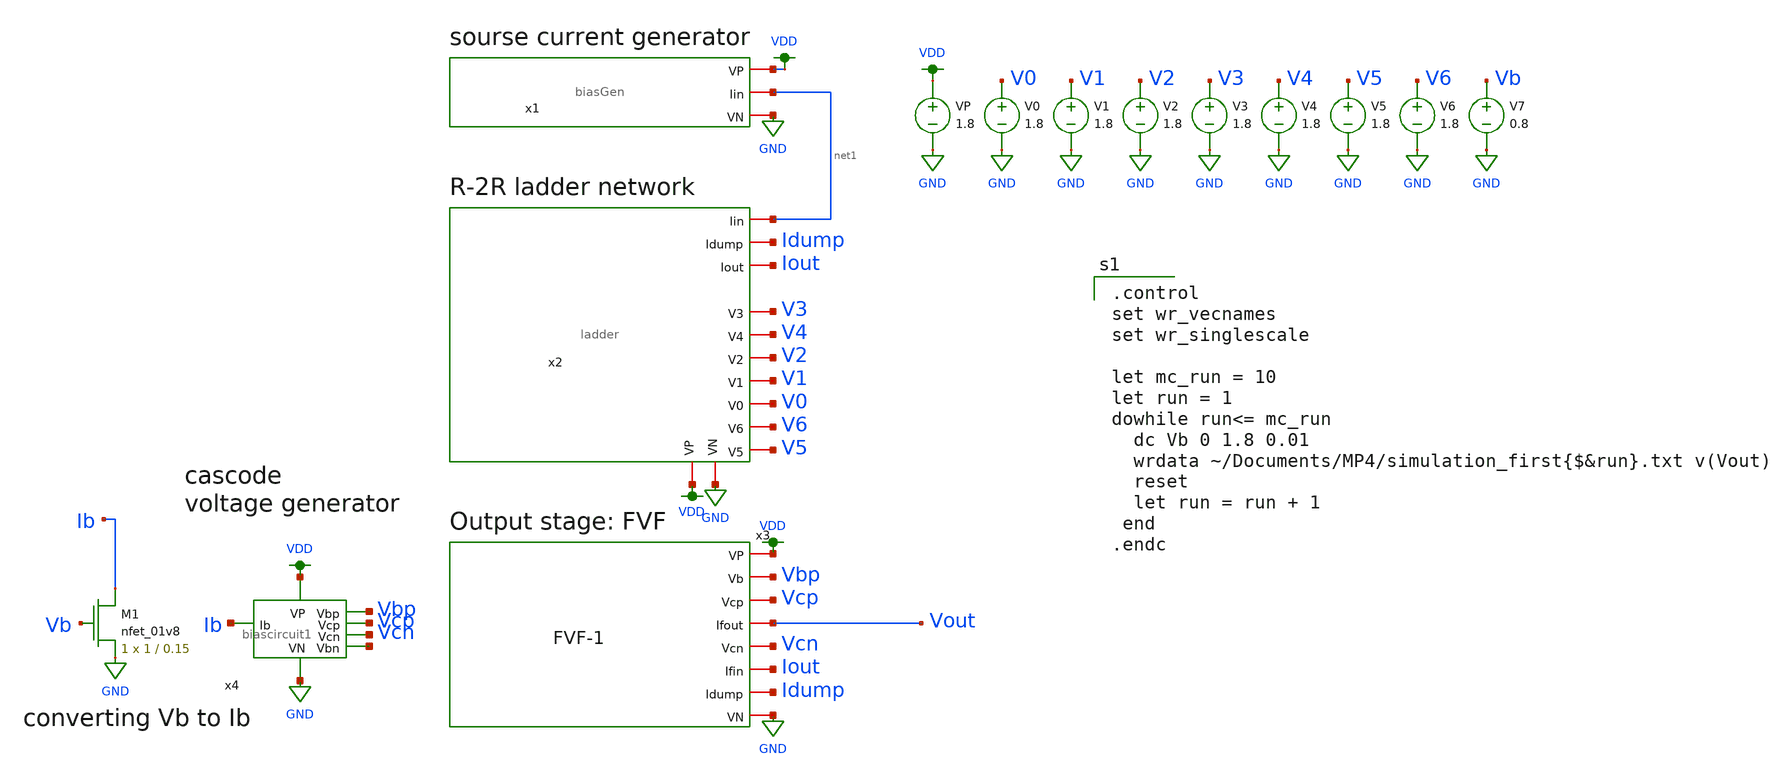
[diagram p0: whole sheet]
** sch_path: MP4-simulation-1.sch
**.subckt MP4-simulation-1
x1 VDD net1 GND biasGen
V1 V1 GND 1.8
V2 V2 GND 1.8
V3 V3 GND 1.8
V4 V4 GND 1.8
V5 V5 GND 1.8
V6 V6 GND 1.8
V0 V0 GND 1.8
VP VDD GND 1.8
V7 Vb GND 0.8
x2 net1 Idump Iout V3 V4 V2 V1 V0 V6 V5 GND VDD ladder
x4 Vbp Vcn Vcp net2 Ib GND VDD biascircuit1
x3 VDD Vbp Vcp Vout Vcn Iout Idump GND FVF-1
XM1 Ib Vb GND GND sky130_fd_pr__nfet_01v8 L=0.15 W=1 nf=1 ad='int((nf+1)/2) * W/nf * 0.29' as='int((nf+2)/2) * W/nf * 0.29'
+ pd='2*int((nf+1)/2) * (W/nf + 0.29)' ps='2*int((nf+2)/2) * (W/nf + 0.29)' nrd='0.29 / W' nrs='0.29 / W'
+ sa=0 sb=0 sd=0 mult=1 m=1
**** begin user architecture code

.option wnflag=1
.param MC_SWITCH=0.0
.lib ~/skywater/skywater-pdk/libraries/sky130_fd_pr_ngspice/latest/models/sky130.lib.spice tt


.control
set wr_vecnames
set wr_singlescale

let mc_run = 10
let run = 1
dowhile run<= mc_run
  dc Vb 0 1.8 0.01
  wrdata ~/Documents/MP4/simulation_first{$&run}.txt v(Vout)
  reset
  let run = run + 1
 end
.endc

**** end user architecture code
**.ends

* expanding   symbol:  ./biasGen.sym # of pins=3
** sym_path: biasGen.sym
** sch_path: biasGen.sch
.subckt biasGen VP Iin VN
*.iopin VN
*.iopin Iin
*.iopin VP
XM1 net4 net4 VN GND sky130_fd_pr__nfet_01v8 L=0.15 W=1 nf=1 ad='int((nf+1)/2) * W/nf * 0.29' as='int((nf+2)/2) * W/nf * 0.29'
+ pd='2*int((nf+1)/2) * (W/nf + 0.29)' ps='2*int((nf+2)/2) * (W/nf + 0.29)' nrd='0.29 / W' nrs='0.29 / W'
+ sa=0 sb=0 sd=0 mult=1 m=1
XM2 VN net4 net3 GND sky130_fd_pr__nfet_01v8 L=0.15 W=1 nf=1 ad='int((nf+1)/2) * W/nf * 0.29' as='int((nf+2)/2) * W/nf * 0.29'
+ pd='2*int((nf+1)/2) * (W/nf + 0.29)' ps='2*int((nf+2)/2) * (W/nf + 0.29)' nrd='0.29 / W' nrs='0.29 / W'
+ sa=0 sb=0 sd=0 mult=1 m=1
XM3 net1 net2 VN GND sky130_fd_pr__nfet_01v8 L=0.15 W=1 nf=1 ad='int((nf+1)/2) * W/nf * 0.29' as='int((nf+2)/2) * W/nf * 0.29'
+ pd='2*int((nf+1)/2) * (W/nf + 0.29)' ps='2*int((nf+2)/2) * (W/nf + 0.29)' nrd='0.29 / W' nrs='0.29 / W'
+ sa=0 sb=0 sd=0 mult=1 m=1
XM4 net5 net2 net2 GND sky130_fd_pr__nfet_01v8 L=0.15 W=8 nf=1 ad='int((nf+1)/2) * W/nf * 0.29' as='int((nf+2)/2) * W/nf * 0.29'
+ pd='2*int((nf+1)/2) * (W/nf + 0.29)' ps='2*int((nf+2)/2) * (W/nf + 0.29)' nrd='0.29 / W' nrs='0.29 / W'
+ sa=0 sb=0 sd=0 mult=1 m=1
XM5 net3 net1 VP VDD sky130_fd_pr__pfet_01v8 L=0.15 W=1 nf=1 ad='int((nf+1)/2) * W/nf * 0.29' as='int((nf+2)/2) * W/nf * 0.29'
+ pd='2*int((nf+1)/2) * (W/nf + 0.29)' ps='2*int((nf+2)/2) * (W/nf + 0.29)' nrd='0.29 / W' nrs='0.29 / W'
+ sa=0 sb=0 sd=0 mult=1 m=1
XM6 VP net1 net1 VDD sky130_fd_pr__pfet_01v8 L=0.15 W=1 nf=1 ad='int((nf+1)/2) * W/nf * 0.29' as='int((nf+2)/2) * W/nf * 0.29'
+ pd='2*int((nf+1)/2) * (W/nf + 0.29)' ps='2*int((nf+2)/2) * (W/nf + 0.29)' nrd='0.29 / W' nrs='0.29 / W'
+ sa=0 sb=0 sd=0 mult=1 m=1
XM7 VP net3 net2 VDD sky130_fd_pr__pfet_01v8 L=0.15 W=1 nf=1 ad='int((nf+1)/2) * W/nf * 0.29' as='int((nf+2)/2) * W/nf * 0.29'
+ pd='2*int((nf+1)/2) * (W/nf + 0.29)' ps='2*int((nf+2)/2) * (W/nf + 0.29)' nrd='0.29 / W' nrs='0.29 / W'
+ sa=0 sb=0 sd=0 mult=1 m=1
XM8 net4 net3 VP VDD sky130_fd_pr__pfet_01v8 L=0.15 W=1 nf=1 ad='int((nf+1)/2) * W/nf * 0.29' as='int((nf+2)/2) * W/nf * 0.29'
+ pd='2*int((nf+1)/2) * (W/nf + 0.29)' ps='2*int((nf+2)/2) * (W/nf + 0.29)' nrd='0.29 / W' nrs='0.29 / W'
+ sa=0 sb=0 sd=0 mult=1 m=1
R1 net5 VN 100k m=1
XM9 Iin net3 VP VDD sky130_fd_pr__pfet_01v8 L=0.15 W=1 nf=1 ad='int((nf+1)/2) * W/nf * 0.29' as='int((nf+2)/2) * W/nf * 0.29'
+ pd='2*int((nf+1)/2) * (W/nf + 0.29)' ps='2*int((nf+2)/2) * (W/nf + 0.29)' nrd='0.29 / W' nrs='0.29 / W'
+ sa=0 sb=0 sd=0 mult=1 m=1
.ends


* expanding   symbol:  ./ladder.sym # of pins=12
** sym_path: ladder.sym
** sch_path: ladder.sch
.subckt ladder Iin Idump Iout V3 V4 V2 V1 V0 V6 V5 VN VP
*.iopin VP
*.iopin Iin
*.iopin V0
*.iopin V1
*.iopin V2
*.iopin V3
*.iopin V4
*.iopin V5
*.iopin V6
*.iopin VN
*.iopin Idump
*.iopin Iout
XM1 Iin VP net1 GND sky130_fd_pr__nfet_01v8 L=0.15 W=1 nf=1 ad='int((nf+1)/2) * W/nf * 0.29' as='int((nf+2)/2) * W/nf * 0.29'
+ pd='2*int((nf+1)/2) * (W/nf + 0.29)' ps='2*int((nf+2)/2) * (W/nf + 0.29)' nrd='0.29 / W' nrs='0.29 / W'
+ sa=0 sb=0 sd=0 mult=1 m=1
XM3 Iin VP net3 GND sky130_fd_pr__nfet_01v8 L=0.15 W=1 nf=1 ad='int((nf+1)/2) * W/nf * 0.29' as='int((nf+2)/2) * W/nf * 0.29'
+ pd='2*int((nf+1)/2) * (W/nf + 0.29)' ps='2*int((nf+2)/2) * (W/nf + 0.29)' nrd='0.29 / W' nrs='0.29 / W'
+ sa=0 sb=0 sd=0 mult=1 m=1
XM5 net3 VP net4 GND sky130_fd_pr__nfet_01v8 L=0.15 W=1 nf=1 ad='int((nf+1)/2) * W/nf * 0.29' as='int((nf+2)/2) * W/nf * 0.29'
+ pd='2*int((nf+1)/2) * (W/nf + 0.29)' ps='2*int((nf+2)/2) * (W/nf + 0.29)' nrd='0.29 / W' nrs='0.29 / W'
+ sa=0 sb=0 sd=0 mult=1 m=1
XM7 net3 VP net6 GND sky130_fd_pr__nfet_01v8 L=0.15 W=1 nf=1 ad='int((nf+1)/2) * W/nf * 0.29' as='int((nf+2)/2) * W/nf * 0.29'
+ pd='2*int((nf+1)/2) * (W/nf + 0.29)' ps='2*int((nf+2)/2) * (W/nf + 0.29)' nrd='0.29 / W' nrs='0.29 / W'
+ sa=0 sb=0 sd=0 mult=1 m=1
XM6 net4 V1 net2 GND sky130_fd_pr__nfet_01v8 L=0.15 W=1 nf=1 ad='int((nf+1)/2) * W/nf * 0.29' as='int((nf+2)/2) * W/nf * 0.29'
+ pd='2*int((nf+1)/2) * (W/nf + 0.29)' ps='2*int((nf+2)/2) * (W/nf + 0.29)' nrd='0.29 / W' nrs='0.29 / W'
+ sa=0 sb=0 sd=0 mult=1 m=1
XM8 net4 net18 net5 GND sky130_fd_pr__nfet_01v8 L=0.15 W=1 nf=1 ad='int((nf+1)/2) * W/nf * 0.29' as='int((nf+2)/2) * W/nf * 0.29'
+ pd='2*int((nf+1)/2) * (W/nf + 0.29)' ps='2*int((nf+2)/2) * (W/nf + 0.29)' nrd='0.29 / W' nrs='0.29 / W'
+ sa=0 sb=0 sd=0 mult=1 m=1
XM2 net1 V0 net2 GND sky130_fd_pr__nfet_01v8 L=0.15 W=1 nf=1 ad='int((nf+1)/2) * W/nf * 0.29' as='int((nf+2)/2) * W/nf * 0.29'
+ pd='2*int((nf+1)/2) * (W/nf + 0.29)' ps='2*int((nf+2)/2) * (W/nf + 0.29)' nrd='0.29 / W' nrs='0.29 / W'
+ sa=0 sb=0 sd=0 mult=1 m=1
XM4 net1 net17 net5 GND sky130_fd_pr__nfet_01v8 L=0.15 W=1 nf=1 ad='int((nf+1)/2) * W/nf * 0.29' as='int((nf+2)/2) * W/nf * 0.29'
+ pd='2*int((nf+1)/2) * (W/nf + 0.29)' ps='2*int((nf+2)/2) * (W/nf + 0.29)' nrd='0.29 / W' nrs='0.29 / W'
+ sa=0 sb=0 sd=0 mult=1 m=1
XM9 net6 VP net7 GND sky130_fd_pr__nfet_01v8 L=0.15 W=1 nf=1 ad='int((nf+1)/2) * W/nf * 0.29' as='int((nf+2)/2) * W/nf * 0.29'
+ pd='2*int((nf+1)/2) * (W/nf + 0.29)' ps='2*int((nf+2)/2) * (W/nf + 0.29)' nrd='0.29 / W' nrs='0.29 / W'
+ sa=0 sb=0 sd=0 mult=1 m=1
XM11 net6 VP net8 GND sky130_fd_pr__nfet_01v8 L=0.15 W=1 nf=1 ad='int((nf+1)/2) * W/nf * 0.29' as='int((nf+2)/2) * W/nf * 0.29'
+ pd='2*int((nf+1)/2) * (W/nf + 0.29)' ps='2*int((nf+2)/2) * (W/nf + 0.29)' nrd='0.29 / W' nrs='0.29 / W'
+ sa=0 sb=0 sd=0 mult=1 m=1
XM10 net7 V2 net2 GND sky130_fd_pr__nfet_01v8 L=0.15 W=1 nf=1 ad='int((nf+1)/2) * W/nf * 0.29' as='int((nf+2)/2) * W/nf * 0.29'
+ pd='2*int((nf+1)/2) * (W/nf + 0.29)' ps='2*int((nf+2)/2) * (W/nf + 0.29)' nrd='0.29 / W' nrs='0.29 / W'
+ sa=0 sb=0 sd=0 mult=1 m=1
XM12 net7 net19 net5 GND sky130_fd_pr__nfet_01v8 L=0.15 W=1 nf=1 ad='int((nf+1)/2) * W/nf * 0.29' as='int((nf+2)/2) * W/nf * 0.29'
+ pd='2*int((nf+1)/2) * (W/nf + 0.29)' ps='2*int((nf+2)/2) * (W/nf + 0.29)' nrd='0.29 / W' nrs='0.29 / W'
+ sa=0 sb=0 sd=0 mult=1 m=1
XM13 net8 VP net9 GND sky130_fd_pr__nfet_01v8 L=0.15 W=1 nf=1 ad='int((nf+1)/2) * W/nf * 0.29' as='int((nf+2)/2) * W/nf * 0.29'
+ pd='2*int((nf+1)/2) * (W/nf + 0.29)' ps='2*int((nf+2)/2) * (W/nf + 0.29)' nrd='0.29 / W' nrs='0.29 / W'
+ sa=0 sb=0 sd=0 mult=1 m=1
XM15 net8 VP net10 GND sky130_fd_pr__nfet_01v8 L=0.15 W=1 nf=1 ad='int((nf+1)/2) * W/nf * 0.29' as='int((nf+2)/2) * W/nf * 0.29'
+ pd='2*int((nf+1)/2) * (W/nf + 0.29)' ps='2*int((nf+2)/2) * (W/nf + 0.29)' nrd='0.29 / W' nrs='0.29 / W'
+ sa=0 sb=0 sd=0 mult=1 m=1
XM14 net9 V3 net2 GND sky130_fd_pr__nfet_01v8 L=0.15 W=1 nf=1 ad='int((nf+1)/2) * W/nf * 0.29' as='int((nf+2)/2) * W/nf * 0.29'
+ pd='2*int((nf+1)/2) * (W/nf + 0.29)' ps='2*int((nf+2)/2) * (W/nf + 0.29)' nrd='0.29 / W' nrs='0.29 / W'
+ sa=0 sb=0 sd=0 mult=1 m=1
XM16 net9 net20 net5 GND sky130_fd_pr__nfet_01v8 L=0.15 W=1 nf=1 ad='int((nf+1)/2) * W/nf * 0.29' as='int((nf+2)/2) * W/nf * 0.29'
+ pd='2*int((nf+1)/2) * (W/nf + 0.29)' ps='2*int((nf+2)/2) * (W/nf + 0.29)' nrd='0.29 / W' nrs='0.29 / W'
+ sa=0 sb=0 sd=0 mult=1 m=1
XM17 net10 VP net11 GND sky130_fd_pr__nfet_01v8 L=0.15 W=1 nf=1 ad='int((nf+1)/2) * W/nf * 0.29' as='int((nf+2)/2) * W/nf * 0.29'
+ pd='2*int((nf+1)/2) * (W/nf + 0.29)' ps='2*int((nf+2)/2) * (W/nf + 0.29)' nrd='0.29 / W' nrs='0.29 / W'
+ sa=0 sb=0 sd=0 mult=1 m=1
XM19 net10 VP net12 GND sky130_fd_pr__nfet_01v8 L=0.15 W=1 nf=1 ad='int((nf+1)/2) * W/nf * 0.29' as='int((nf+2)/2) * W/nf * 0.29'
+ pd='2*int((nf+1)/2) * (W/nf + 0.29)' ps='2*int((nf+2)/2) * (W/nf + 0.29)' nrd='0.29 / W' nrs='0.29 / W'
+ sa=0 sb=0 sd=0 mult=1 m=1
XM18 net11 V4 net2 GND sky130_fd_pr__nfet_01v8 L=0.15 W=1 nf=1 ad='int((nf+1)/2) * W/nf * 0.29' as='int((nf+2)/2) * W/nf * 0.29'
+ pd='2*int((nf+1)/2) * (W/nf + 0.29)' ps='2*int((nf+2)/2) * (W/nf + 0.29)' nrd='0.29 / W' nrs='0.29 / W'
+ sa=0 sb=0 sd=0 mult=1 m=1
XM20 net11 net21 net5 GND sky130_fd_pr__nfet_01v8 L=0.15 W=1 nf=1 ad='int((nf+1)/2) * W/nf * 0.29' as='int((nf+2)/2) * W/nf * 0.29'
+ pd='2*int((nf+1)/2) * (W/nf + 0.29)' ps='2*int((nf+2)/2) * (W/nf + 0.29)' nrd='0.29 / W' nrs='0.29 / W'
+ sa=0 sb=0 sd=0 mult=1 m=1
XM21 net12 VP net13 GND sky130_fd_pr__nfet_01v8 L=0.15 W=1 nf=1 ad='int((nf+1)/2) * W/nf * 0.29' as='int((nf+2)/2) * W/nf * 0.29'
+ pd='2*int((nf+1)/2) * (W/nf + 0.29)' ps='2*int((nf+2)/2) * (W/nf + 0.29)' nrd='0.29 / W' nrs='0.29 / W'
+ sa=0 sb=0 sd=0 mult=1 m=1
XM23 net12 VP net14 GND sky130_fd_pr__nfet_01v8 L=0.15 W=1 nf=1 ad='int((nf+1)/2) * W/nf * 0.29' as='int((nf+2)/2) * W/nf * 0.29'
+ pd='2*int((nf+1)/2) * (W/nf + 0.29)' ps='2*int((nf+2)/2) * (W/nf + 0.29)' nrd='0.29 / W' nrs='0.29 / W'
+ sa=0 sb=0 sd=0 mult=1 m=1
XM22 net13 V5 net2 GND sky130_fd_pr__nfet_01v8 L=0.15 W=1 nf=1 ad='int((nf+1)/2) * W/nf * 0.29' as='int((nf+2)/2) * W/nf * 0.29'
+ pd='2*int((nf+1)/2) * (W/nf + 0.29)' ps='2*int((nf+2)/2) * (W/nf + 0.29)' nrd='0.29 / W' nrs='0.29 / W'
+ sa=0 sb=0 sd=0 mult=1 m=1
XM24 net13 net22 net5 GND sky130_fd_pr__nfet_01v8 L=0.15 W=1 nf=1 ad='int((nf+1)/2) * W/nf * 0.29' as='int((nf+2)/2) * W/nf * 0.29'
+ pd='2*int((nf+1)/2) * (W/nf + 0.29)' ps='2*int((nf+2)/2) * (W/nf + 0.29)' nrd='0.29 / W' nrs='0.29 / W'
+ sa=0 sb=0 sd=0 mult=1 m=1
XM25 net14 VP net15 GND sky130_fd_pr__nfet_01v8 L=0.15 W=1 nf=1 ad='int((nf+1)/2) * W/nf * 0.29' as='int((nf+2)/2) * W/nf * 0.29'
+ pd='2*int((nf+1)/2) * (W/nf + 0.29)' ps='2*int((nf+2)/2) * (W/nf + 0.29)' nrd='0.29 / W' nrs='0.29 / W'
+ sa=0 sb=0 sd=0 mult=1 m=1
XM27 net14 VP net16 GND sky130_fd_pr__nfet_01v8 L=0.15 W=1 nf=1 ad='int((nf+1)/2) * W/nf * 0.29' as='int((nf+2)/2) * W/nf * 0.29'
+ pd='2*int((nf+1)/2) * (W/nf + 0.29)' ps='2*int((nf+2)/2) * (W/nf + 0.29)' nrd='0.29 / W' nrs='0.29 / W'
+ sa=0 sb=0 sd=0 mult=1 m=1
XM26 net15 V6 net2 GND sky130_fd_pr__nfet_01v8 L=0.15 W=1 nf=1 ad='int((nf+1)/2) * W/nf * 0.29' as='int((nf+2)/2) * W/nf * 0.29'
+ pd='2*int((nf+1)/2) * (W/nf + 0.29)' ps='2*int((nf+2)/2) * (W/nf + 0.29)' nrd='0.29 / W' nrs='0.29 / W'
+ sa=0 sb=0 sd=0 mult=1 m=1
XM28 net15 net23 net5 GND sky130_fd_pr__nfet_01v8 L=0.15 W=1 nf=1 ad='int((nf+1)/2) * W/nf * 0.29' as='int((nf+2)/2) * W/nf * 0.29'
+ pd='2*int((nf+1)/2) * (W/nf + 0.29)' ps='2*int((nf+2)/2) * (W/nf + 0.29)' nrd='0.29 / W' nrs='0.29 / W'
+ sa=0 sb=0 sd=0 mult=1 m=1
XM29 net16 VP net5 GND sky130_fd_pr__nfet_01v8 L=0.15 W=1 nf=1 ad='int((nf+1)/2) * W/nf * 0.29' as='int((nf+2)/2) * W/nf * 0.29'
+ pd='2*int((nf+1)/2) * (W/nf + 0.29)' ps='2*int((nf+2)/2) * (W/nf + 0.29)' nrd='0.29 / W' nrs='0.29 / W'
+ sa=0 sb=0 sd=0 mult=1 m=1
x1 net17 V0 VP VN inverter
x2 net18 V1 VP VN inverter
x3 net19 V2 VP VN inverter
x4 net20 V3 VP VN inverter
x5 net21 V4 VP VN inverter
x6 net22 V5 VP VN inverter
x7 net23 V6 VP VN inverter
XM30 VN net5 net5 GND sky130_fd_pr__nfet_01v8 L=0.15 W=1 nf=1 ad='int((nf+1)/2) * W/nf * 0.29' as='int((nf+2)/2) * W/nf * 0.29'
+ pd='2*int((nf+1)/2) * (W/nf + 0.29)' ps='2*int((nf+2)/2) * (W/nf + 0.29)' nrd='0.29 / W' nrs='0.29 / W'
+ sa=0 sb=0 sd=0 mult=1 m=1
XM31 VN net2 net2 GND sky130_fd_pr__nfet_01v8 L=0.15 W=1 nf=1 ad='int((nf+1)/2) * W/nf * 0.29' as='int((nf+2)/2) * W/nf * 0.29'
+ pd='2*int((nf+1)/2) * (W/nf + 0.29)' ps='2*int((nf+2)/2) * (W/nf + 0.29)' nrd='0.29 / W' nrs='0.29 / W'
+ sa=0 sb=0 sd=0 mult=1 m=1
XM32 Idump net5 VN GND sky130_fd_pr__nfet_01v8 L=0.15 W=1 nf=1 ad='int((nf+1)/2) * W/nf * 0.29' as='int((nf+2)/2) * W/nf * 0.29'
+ pd='2*int((nf+1)/2) * (W/nf + 0.29)' ps='2*int((nf+2)/2) * (W/nf + 0.29)' nrd='0.29 / W' nrs='0.29 / W'
+ sa=0 sb=0 sd=0 mult=1 m=1
XM33 Iout net2 VN GND sky130_fd_pr__nfet_01v8 L=0.15 W=1 nf=1 ad='int((nf+1)/2) * W/nf * 0.29' as='int((nf+2)/2) * W/nf * 0.29'
+ pd='2*int((nf+1)/2) * (W/nf + 0.29)' ps='2*int((nf+2)/2) * (W/nf + 0.29)' nrd='0.29 / W' nrs='0.29 / W'
+ sa=0 sb=0 sd=0 mult=1 m=1
.ends


* expanding   symbol:  ./biascircuit1.sym # of pins=7
** sym_path: biascircuit1.sym
** sch_path: biascircuit1.sch
.subckt biascircuit1 Vbp Vcn Vcp Vbn Ib VN VP
*.iopin VP
*.iopin Ib
*.iopin VN
*.iopin Vcp
*.iopin Vbp
*.iopin Vbn
*.iopin Vcn
XM5 Vbn Vbn net1 GND sky130_fd_pr__nfet_01v8 L=0.5 W=24 nf=1 ad='int((nf+1)/2) * W/nf * 0.29' as='int((nf+2)/2) * W/nf * 0.29'
+ pd='2*int((nf+1)/2) * (W/nf + 0.29)' ps='2*int((nf+2)/2) * (W/nf + 0.29)' nrd='0.29 / W' nrs='0.29 / W'
+ sa=0 sb=0 sd=0 mult=1 m=1
XM6 net1 Vbn VN GND sky130_fd_pr__nfet_01v8 L=0.5 W=12 nf=1 ad='int((nf+1)/2) * W/nf * 0.29' as='int((nf+2)/2) * W/nf * 0.29'
+ pd='2*int((nf+1)/2) * (W/nf + 0.29)' ps='2*int((nf+2)/2) * (W/nf + 0.29)' nrd='0.29 / W' nrs='0.29 / W'
+ sa=0 sb=0 sd=0 mult=1 m=1
XM4 net1 Vcn Vcn GND sky130_fd_pr__nfet_01v8 L=0.5 W=12 nf=1 ad='int((nf+1)/2) * W/nf * 0.29' as='int((nf+2)/2) * W/nf * 0.29'
+ pd='2*int((nf+1)/2) * (W/nf + 0.29)' ps='2*int((nf+2)/2) * (W/nf + 0.29)' nrd='0.29 / W' nrs='0.29 / W'
+ sa=0 sb=0 sd=0 mult=1 m=1
XM1 VP net2 Vbn VDD sky130_fd_pr__pfet_01v8 L=0.5 W=6 nf=1 ad='int((nf+1)/2) * W/nf * 0.29' as='int((nf+2)/2) * W/nf * 0.29'
+ pd='2*int((nf+1)/2) * (W/nf + 0.29)' ps='2*int((nf+2)/2) * (W/nf + 0.29)' nrd='0.29 / W' nrs='0.29 / W'
+ sa=0 sb=0 sd=0 mult=1 m=1
XM2 VP net2 Vcn VDD sky130_fd_pr__pfet_01v8 L=0.5 W=12 nf=1 ad='int((nf+1)/2) * W/nf * 0.29' as='int((nf+2)/2) * W/nf * 0.29'
+ pd='2*int((nf+1)/2) * (W/nf + 0.29)' ps='2*int((nf+2)/2) * (W/nf + 0.29)' nrd='0.29 / W' nrs='0.29 / W'
+ sa=0 sb=0 sd=0 mult=1 m=1
XM3 net2 net2 VP VDD sky130_fd_pr__pfet_01v8 L=0.5 W=12 nf=1 ad='int((nf+1)/2) * W/nf * 0.29' as='int((nf+2)/2) * W/nf * 0.29'
+ pd='2*int((nf+1)/2) * (W/nf + 0.29)' ps='2*int((nf+2)/2) * (W/nf + 0.29)' nrd='0.29 / W' nrs='0.29 / W'
+ sa=0 sb=0 sd=0 mult=1 m=1
XM9 Vbp Vbp net3 VDD sky130_fd_pr__pfet_01v8 L=0.5 W=24 nf=1 ad='int((nf+1)/2) * W/nf * 0.29' as='int((nf+2)/2) * W/nf * 0.29'
+ pd='2*int((nf+1)/2) * (W/nf + 0.29)' ps='2*int((nf+2)/2) * (W/nf + 0.29)' nrd='0.29 / W' nrs='0.29 / W'
+ sa=0 sb=0 sd=0 mult=1 m=1
XM11 VN Ib Vcp GND sky130_fd_pr__nfet_01v8 L=0.5 W=12 nf=1 ad='int((nf+1)/2) * W/nf * 0.29' as='int((nf+2)/2) * W/nf * 0.29'
+ pd='2*int((nf+1)/2) * (W/nf + 0.29)' ps='2*int((nf+2)/2) * (W/nf + 0.29)' nrd='0.29 / W' nrs='0.29 / W'
+ sa=0 sb=0 sd=0 mult=1 m=1
XM10 net2 Ib VN GND sky130_fd_pr__nfet_01v8 L=0.5 W=12 nf=1 ad='int((nf+1)/2) * W/nf * 0.29' as='int((nf+2)/2) * W/nf * 0.29'
+ pd='2*int((nf+1)/2) * (W/nf + 0.29)' ps='2*int((nf+2)/2) * (W/nf + 0.29)' nrd='0.29 / W' nrs='0.29 / W'
+ sa=0 sb=0 sd=0 mult=1 m=1
XM8 net3 Vcp Vcp VDD sky130_fd_pr__pfet_01v8 L=0.5 W=12 nf=1 ad='int((nf+1)/2) * W/nf * 0.29' as='int((nf+2)/2) * W/nf * 0.29'
+ pd='2*int((nf+1)/2) * (W/nf + 0.29)' ps='2*int((nf+2)/2) * (W/nf + 0.29)' nrd='0.29 / W' nrs='0.29 / W'
+ sa=0 sb=0 sd=0 mult=1 m=1
XM12 VN Ib Vbp GND sky130_fd_pr__nfet_01v8 L=0.5 W=6 nf=1 ad='int((nf+1)/2) * W/nf * 0.29' as='int((nf+2)/2) * W/nf * 0.29'
+ pd='2*int((nf+1)/2) * (W/nf + 0.29)' ps='2*int((nf+2)/2) * (W/nf + 0.29)' nrd='0.29 / W' nrs='0.29 / W'
+ sa=0 sb=0 sd=0 mult=1 m=1
XM13 VN Ib Ib GND sky130_fd_pr__nfet_01v8 L=0.5 W=12 nf=1 ad='int((nf+1)/2) * W/nf * 0.29' as='int((nf+2)/2) * W/nf * 0.29'
+ pd='2*int((nf+1)/2) * (W/nf + 0.29)' ps='2*int((nf+2)/2) * (W/nf + 0.29)' nrd='0.29 / W' nrs='0.29 / W'
+ sa=0 sb=0 sd=0 mult=1 m=1
XM7 net3 Vbp VP VDD sky130_fd_pr__pfet_01v8 L=0.5 W=12 nf=1 ad='int((nf+1)/2) * W/nf * 0.29' as='int((nf+2)/2) * W/nf * 0.29'
+ pd='2*int((nf+1)/2) * (W/nf + 0.29)' ps='2*int((nf+2)/2) * (W/nf + 0.29)' nrd='0.29 / W' nrs='0.29 / W'
+ sa=0 sb=0 sd=0 mult=1 m=1
.ends


* expanding   symbol:  ./FVF-1.sym # of pins=8
** sym_path: FVF-1.sym
** sch_path: FVF-1.sch
.subckt FVF-1 VP Vb Vcp Ifout Vcn Ifin Idump VN
*.iopin VN
*.iopin Vcn
*.iopin Ifin
*.iopin Idump
*.iopin Vcp
*.iopin VP
*.iopin Vb
*.opin Ifout
XM1 net1 Vcn Idump GND sky130_fd_pr__nfet_01v8 L=0.15 W=1 nf=1 ad='int((nf+1)/2) * W/nf * 0.29' as='int((nf+2)/2) * W/nf * 0.29'
+ pd='2*int((nf+1)/2) * (W/nf + 0.29)' ps='2*int((nf+2)/2) * (W/nf + 0.29)' nrd='0.29 / W' nrs='0.29 / W'
+ sa=0 sb=0 sd=0 mult=1 m=1
XM2 VN net1 Idump GND sky130_fd_pr__nfet_01v8 L=0.15 W=1 nf=1 ad='int((nf+1)/2) * W/nf * 0.29' as='int((nf+2)/2) * W/nf * 0.29'
+ pd='2*int((nf+1)/2) * (W/nf + 0.29)' ps='2*int((nf+2)/2) * (W/nf + 0.29)' nrd='0.29 / W' nrs='0.29 / W'
+ sa=0 sb=0 sd=0 mult=1 m=1
XM3 net2 Vcn Ifin GND sky130_fd_pr__nfet_01v8 L=0.15 W=1 nf=1 ad='int((nf+1)/2) * W/nf * 0.29' as='int((nf+2)/2) * W/nf * 0.29'
+ pd='2*int((nf+1)/2) * (W/nf + 0.29)' ps='2*int((nf+2)/2) * (W/nf + 0.29)' nrd='0.29 / W' nrs='0.29 / W'
+ sa=0 sb=0 sd=0 mult=1 m=1
XM4 VN net2 Ifin GND sky130_fd_pr__nfet_01v8 L=0.15 W=1 nf=1 ad='int((nf+1)/2) * W/nf * 0.29' as='int((nf+2)/2) * W/nf * 0.29'
+ pd='2*int((nf+1)/2) * (W/nf + 0.29)' ps='2*int((nf+2)/2) * (W/nf + 0.29)' nrd='0.29 / W' nrs='0.29 / W'
+ sa=0 sb=0 sd=0 mult=1 m=1
XM5 Ifout Vcn net3 GND sky130_fd_pr__nfet_01v8 L=0.15 W=1 nf=1 ad='int((nf+1)/2) * W/nf * 0.29' as='int((nf+2)/2) * W/nf * 0.29'
+ pd='2*int((nf+1)/2) * (W/nf + 0.29)' ps='2*int((nf+2)/2) * (W/nf + 0.29)' nrd='0.29 / W' nrs='0.29 / W'
+ sa=0 sb=0 sd=0 mult=1 m=1
XM6 net3 net2 VN GND sky130_fd_pr__nfet_01v8 L=0.15 W=1 nf=1 ad='int((nf+1)/2) * W/nf * 0.29' as='int((nf+2)/2) * W/nf * 0.29'
+ pd='2*int((nf+1)/2) * (W/nf + 0.29)' ps='2*int((nf+2)/2) * (W/nf + 0.29)' nrd='0.29 / W' nrs='0.29 / W'
+ sa=0 sb=0 sd=0 mult=1 m=1
XM7 net1 Vcp net4 VDD sky130_fd_pr__pfet_01v8 L=0.15 W=1 nf=1 ad='int((nf+1)/2) * W/nf * 0.29' as='int((nf+2)/2) * W/nf * 0.29'
+ pd='2*int((nf+1)/2) * (W/nf + 0.29)' ps='2*int((nf+2)/2) * (W/nf + 0.29)' nrd='0.29 / W' nrs='0.29 / W'
+ sa=0 sb=0 sd=0 mult=1 m=1
XM8 net2 Vcp net5 VDD sky130_fd_pr__pfet_01v8 L=0.15 W=1 nf=1 ad='int((nf+1)/2) * W/nf * 0.29' as='int((nf+2)/2) * W/nf * 0.29'
+ pd='2*int((nf+1)/2) * (W/nf + 0.29)' ps='2*int((nf+2)/2) * (W/nf + 0.29)' nrd='0.29 / W' nrs='0.29 / W'
+ sa=0 sb=0 sd=0 mult=1 m=1
XM9 Ifout Vcp net6 VDD sky130_fd_pr__pfet_01v8 L=0.15 W=1 nf=1 ad='int((nf+1)/2) * W/nf * 0.29' as='int((nf+2)/2) * W/nf * 0.29'
+ pd='2*int((nf+1)/2) * (W/nf + 0.29)' ps='2*int((nf+2)/2) * (W/nf + 0.29)' nrd='0.29 / W' nrs='0.29 / W'
+ sa=0 sb=0 sd=0 mult=1 m=1
XM15 net4 Vb VP VDD sky130_fd_pr__pfet_01v8 L=0.15 W=1 nf=1 ad='int((nf+1)/2) * W/nf * 0.29' as='int((nf+2)/2) * W/nf * 0.29'
+ pd='2*int((nf+1)/2) * (W/nf + 0.29)' ps='2*int((nf+2)/2) * (W/nf + 0.29)' nrd='0.29 / W' nrs='0.29 / W'
+ sa=0 sb=0 sd=0 mult=1 m=1
XM16 net5 Vb VP VDD sky130_fd_pr__pfet_01v8 L=0.15 W=1 nf=1 ad='int((nf+1)/2) * W/nf * 0.29' as='int((nf+2)/2) * W/nf * 0.29'
+ pd='2*int((nf+1)/2) * (W/nf + 0.29)' ps='2*int((nf+2)/2) * (W/nf + 0.29)' nrd='0.29 / W' nrs='0.29 / W'
+ sa=0 sb=0 sd=0 mult=1 m=1
XM17 net6 Vb VP VDD sky130_fd_pr__pfet_01v8 L=0.15 W=1 nf=1 ad='int((nf+1)/2) * W/nf * 0.29' as='int((nf+2)/2) * W/nf * 0.29'
+ pd='2*int((nf+1)/2) * (W/nf + 0.29)' ps='2*int((nf+2)/2) * (W/nf + 0.29)' nrd='0.29 / W' nrs='0.29 / W'
+ sa=0 sb=0 sd=0 mult=1 m=1
.ends


* expanding   symbol:  /home/madvlsi/Documents/MP1/Schematics/inverter.sym # of pins=4
** sym_path: inverter.sym
** sch_path: inverter.sch
.subckt inverter Y A VP VN
*.ipin A
*.opin Y
*.iopin VP
*.iopin VN
XM1 Y A VP VP sky130_fd_pr__pfet_01v8 L=0.15 W=1 nf=1 ad='int((nf+1)/2) * W/nf * 0.29' as='int((nf+2)/2) * W/nf * 0.29'
+ pd='2*int((nf+1)/2) * (W/nf + 0.29)' ps='2*int((nf+2)/2) * (W/nf + 0.29)' nrd='0.29 / W' nrs='0.29 / W'
+ sa=0 sb=0 sd=0 mult=1 m=1
XM2 Y A VN VN sky130_fd_pr__nfet_01v8 L=0.15 W=1 nf=1 ad='int((nf+1)/2) * W/nf * 0.29' as='int((nf+2)/2) * W/nf * 0.29'
+ pd='2*int((nf+1)/2) * (W/nf + 0.29)' ps='2*int((nf+2)/2) * (W/nf + 0.29)' nrd='0.29 / W' nrs='0.29 / W'
+ sa=0 sb=0 sd=0 mult=1 m=1
.ends

.GLOBAL GND
.GLOBAL VDD
.end
